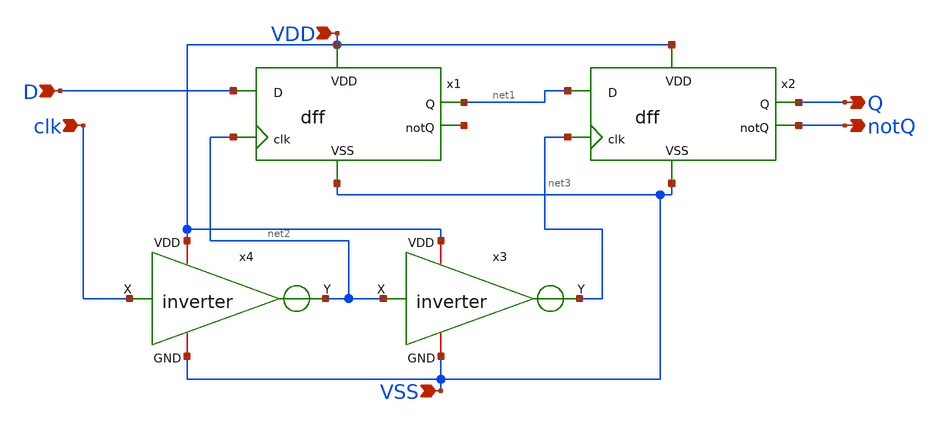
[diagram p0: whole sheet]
** sch_path: Layouts and Schematics/Spice Sim and Schem/etdff.sch
**.subckt etdff VDD Q notQ VSS D clk
*.ipin VDD
*.opin Q
*.opin notQ
*.ipin VSS
*.ipin D
*.ipin clk
x1 VDD net2 net1 D net4 VSS dff
x2 VDD net3 Q net1 notQ VSS dff
x3 VDD net2 net3 VSS inv
x4 VDD clk net2 VSS inv
**.ends
.end
